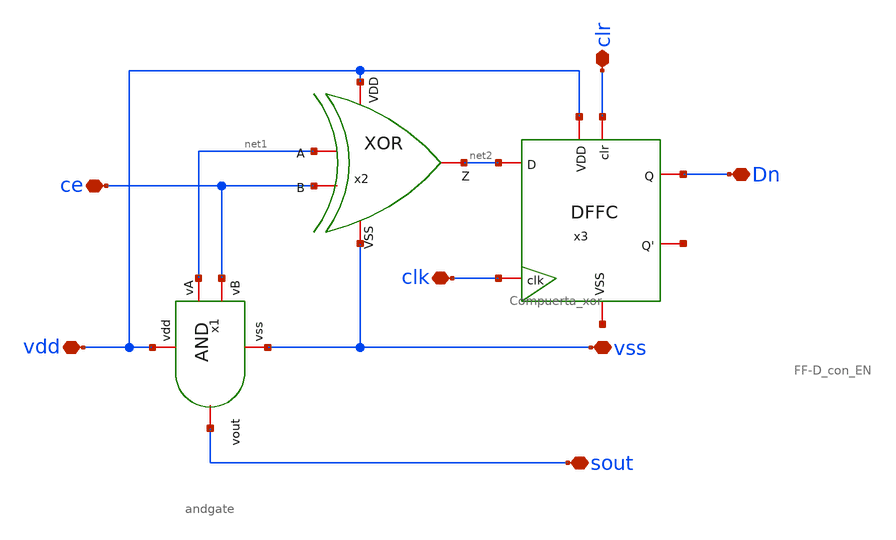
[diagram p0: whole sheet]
** sch_path: design/blocks/count1bit/schematic/counter1bit.sch
**.subckt counter1bit Dn clr sout clk ce vss vdd
*.iopin Dn
*.iopin clr
*.iopin sout
*.iopin clk
*.iopin ce
*.iopin vss
*.iopin vdd
x1 vdd ce net1 sout vss andgate
x2 vdd net2 ce vss net1 Compuerta_xor
x3 clk clr vdd net3 net2 Dn net4 FF-D_con_EN
**.ends
.end
